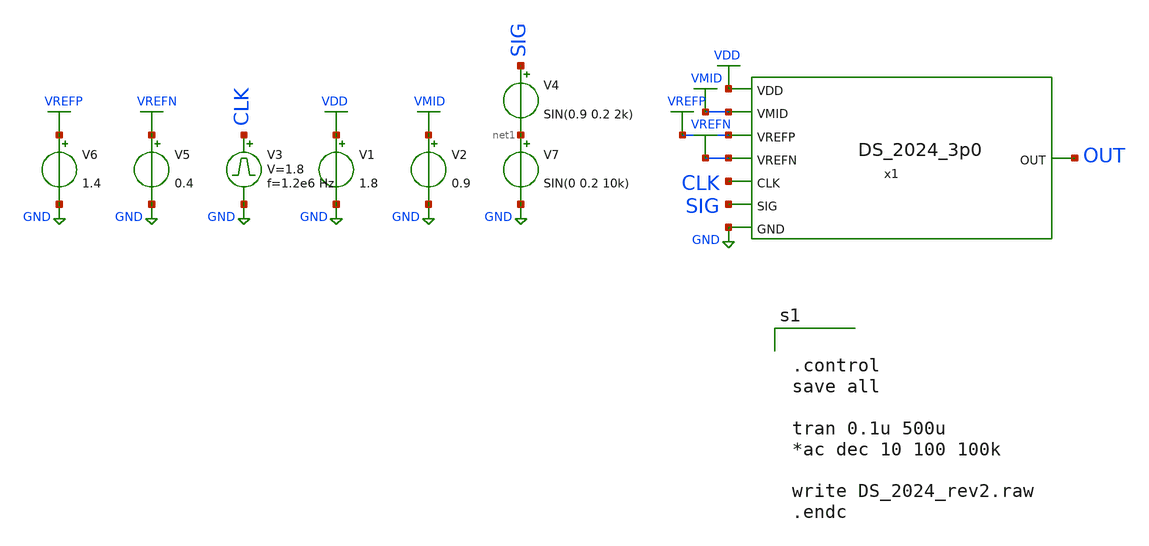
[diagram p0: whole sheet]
** sch_path: DeltaSigma/xschem/DS_2024_Bench.sch
.lib $::SKYWATER_MODELS/sky130.lib.spice tt
.include $::SKYWATER_STDCELLS/sky130_fd_sc_hd.spice

**.subckt DS_2024_Bench
V1 VDD GND 1.8
V2 VMID GND 0.9
V3 CLK GND pulse 0 1.8 '0.495/ 1.2e6 ' '0.01/1.2e6 ' '0.01/1.2e6 ' '0.49/1.2e6 ' '1/1.2e6 '
V4 SIG net1 SIN(0.9 0.2 2k)
V5 VREFN GND 0.4
V6 VREFP GND 1.4
x1 VDD VMID OUT VREFP VREFN GND SIG CLK DS_2024_3p0
V7 net1 GND SIN(0 0.2 10k)
**** begin user architecture code


.control
save all

tran 0.1u 500u
*ac dec 10 100 100k

write DS_2024_rev2.raw
.endc


**** end user architecture code
**.ends
.GLOBAL VDD
.GLOBAL GND
.GLOBAL VMID
.GLOBAL VREFN
.GLOBAL VREFP
.end
